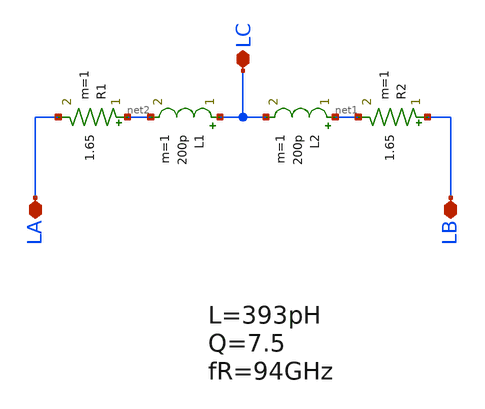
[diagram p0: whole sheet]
** sch_path: xschem/iruwbtx7_tank_inductor.sch
**.subckt iruwbtx7_tank_inductor LC LA LB
*.iopin LC
*.iopin LA
*.iopin LB
L1 LC net2 200p m=1
L2 net1 LC 200p m=1
R1 net2 LA 1.65 m=1
R2 LB net1 1.65 m=1
**.ends
.end
